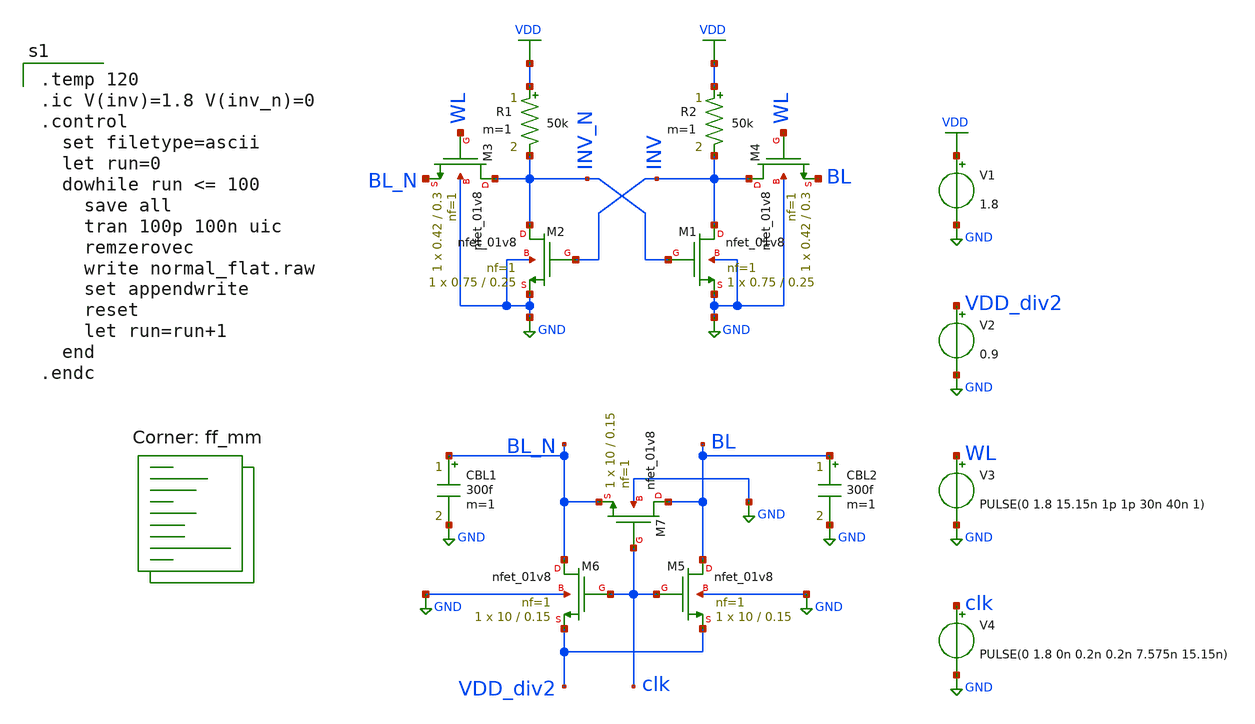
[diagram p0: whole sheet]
** sch_path: analog/schematics/normal_flat.sch
**.subckt normal_flat
XM1 INV INV_N GND GND sky130_fd_pr__nfet_01v8 L=0.25 W=0.75 nf=1 ad='int((nf+1)/2) * W/nf * 0.29' as='int((nf+2)/2) * W/nf * 0.29'
+ pd='2*int((nf+1)/2) * (W/nf + 0.29)' ps='2*int((nf+2)/2) * (W/nf + 0.29)' nrd='0.29 / W' nrs='0.29 / W'
+ sa=0 sb=0 sd=0 mult=1 m=1
R1 VDD INV_N 50k m=1
R2 VDD INV 50k m=1
XM3 INV_N WL BL_N GND sky130_fd_pr__nfet_01v8 L=0.3 W=0.42 nf=1 ad='int((nf+1)/2) * W/nf * 0.29' as='int((nf+2)/2) * W/nf * 0.29'
+ pd='2*int((nf+1)/2) * (W/nf + 0.29)' ps='2*int((nf+2)/2) * (W/nf + 0.29)' nrd='0.29 / W' nrs='0.29 / W'
+ sa=0 sb=0 sd=0 mult=1 m=1
XM4 INV WL BL GND sky130_fd_pr__nfet_01v8 L=0.3 W=0.42 nf=1 ad='int((nf+1)/2) * W/nf * 0.29' as='int((nf+2)/2) * W/nf * 0.29'
+ pd='2*int((nf+1)/2) * (W/nf + 0.29)' ps='2*int((nf+2)/2) * (W/nf + 0.29)' nrd='0.29 / W' nrs='0.29 / W'
+ sa=0 sb=0 sd=0 mult=1 m=1
V1 VDD GND 1.8
V2 VDD_div2 GND 0.9
V3 WL GND PULSE(0 1.8 15.15n 1p 1p 30n 40n 1)
V4 clk GND PULSE(0 1.8 0n 0.2n 0.2n 7.575n 15.15n)
XM2 INV_N INV GND GND sky130_fd_pr__nfet_01v8 L=0.25 W=0.75 nf=1 ad='int((nf+1)/2) * W/nf * 0.29' as='int((nf+2)/2) * W/nf * 0.29'
+ pd='2*int((nf+1)/2) * (W/nf + 0.29)' ps='2*int((nf+2)/2) * (W/nf + 0.29)' nrd='0.29 / W' nrs='0.29 / W'
+ sa=0 sb=0 sd=0 mult=1 m=1
XM5 BL clk VDD_div2 GND sky130_fd_pr__nfet_01v8 L=0.15 W=10 nf=1 ad='int((nf+1)/2) * W/nf * 0.29' as='int((nf+2)/2) * W/nf * 0.29'
+ pd='2*int((nf+1)/2) * (W/nf + 0.29)' ps='2*int((nf+2)/2) * (W/nf + 0.29)' nrd='0.29 / W' nrs='0.29 / W'
+ sa=0 sb=0 sd=0 mult=1 m=1
XM6 BL_N clk VDD_div2 GND sky130_fd_pr__nfet_01v8 L=0.15 W=10 nf=1 ad='int((nf+1)/2) * W/nf * 0.29' as='int((nf+2)/2) * W/nf * 0.29'
+ pd='2*int((nf+1)/2) * (W/nf + 0.29)' ps='2*int((nf+2)/2) * (W/nf + 0.29)' nrd='0.29 / W' nrs='0.29 / W'
+ sa=0 sb=0 sd=0 mult=1 m=1
XM7 BL clk BL_N GND sky130_fd_pr__nfet_01v8 L=0.15 W=10 nf=1 ad='int((nf+1)/2) * W/nf * 0.29' as='int((nf+2)/2) * W/nf * 0.29'
+ pd='2*int((nf+1)/2) * (W/nf + 0.29)' ps='2*int((nf+2)/2) * (W/nf + 0.29)' nrd='0.29 / W' nrs='0.29 / W'
+ sa=0 sb=0 sd=0 mult=1 m=1
CBL1 BL_N GND 300f m=1
CBL2 BL GND 300f m=1
**** begin user architecture code

.temp 120
.ic V(inv)=1.8 V(inv_n)=0
.control
  set filetype=ascii
  let run=0
  dowhile run <= 100
    save all
    tran 100p 100n uic
    remzerovec
    write normal_flat.raw
    set appendwrite
    reset
    let run=run+1
  end
.endc

.lib $::SKYWATER_MODELS/sky130.lib.spice ff_mm
**** end user architecture code
**.ends
.GLOBAL VDD
.GLOBAL GND
.end
